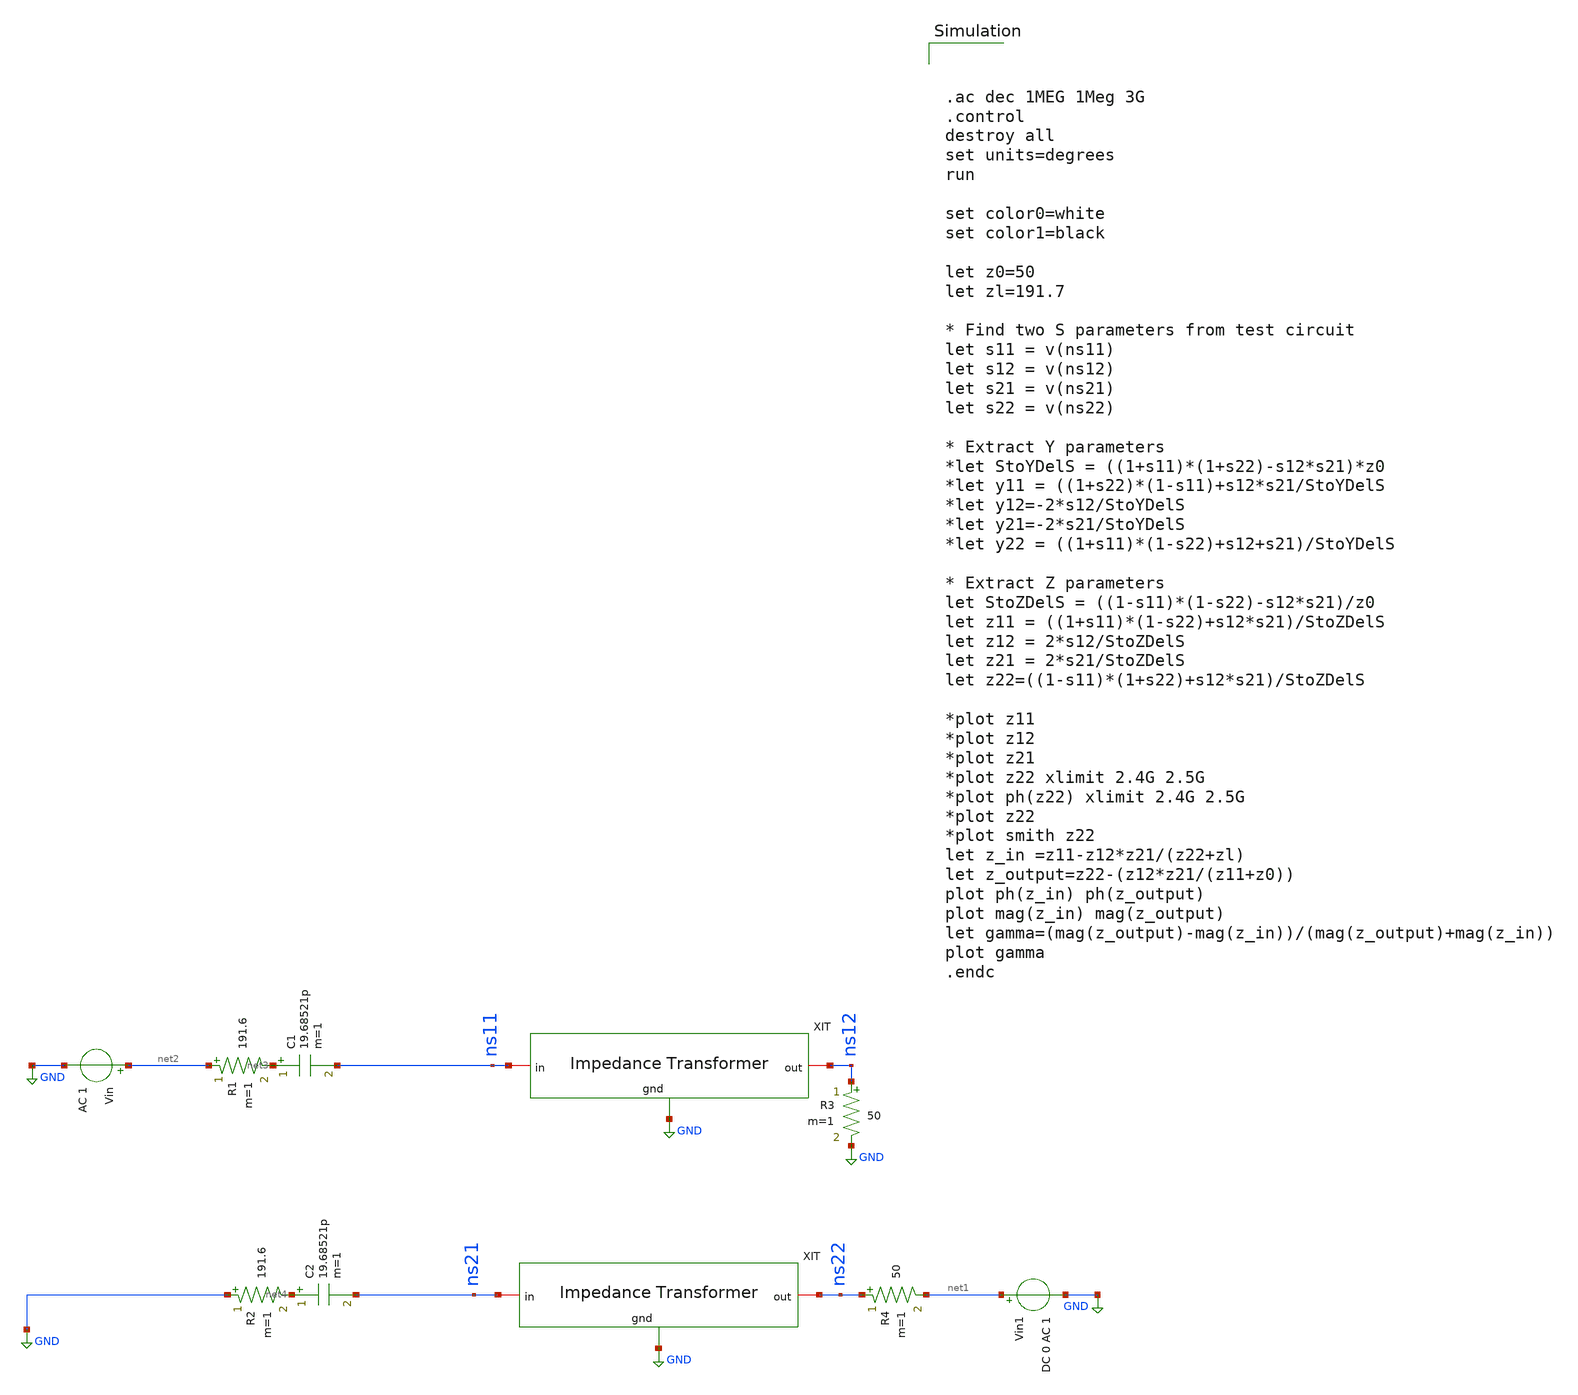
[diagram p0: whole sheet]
** sch_path: impedance-transformer/xschem/impedance-transformer_tb-ac.sch
**.subckt impedance-transformer_tb-ac
Vin1 net1 GND DC 0 AC 1
R3 ns12 GND 50 m=1
R4 ns22 net1 50 m=1
Vin net2 GND AC 1
R1 net2 net3 191.6 m=1
C1 net3 ns11 19.68521p m=1
R2 GND net4 191.6 m=1
C2 net4 ns21 19.68521p m=1
x1 ns11 ns12 GND impedance-transformer
x2 ns21 ns22 GND impedance-transformer
**** begin user architecture code



.ac dec 1MEG 1Meg 3G
.control
destroy all
set units=degrees
run

set color0=white
set color1=black

let z0=50
let zl=191.7

* Find two S parameters from test circuit
let s11 = v(ns11)
let s12 = v(ns12)
let s21 = v(ns21)
let s22 = v(ns22)

* Extract Y parameters
*let StoYDelS = ((1+s11)*(1+s22)-s12*s21)*z0
*let y11 = ((1+s22)*(1-s11)+s12*s21/StoYDelS
*let y12=-2*s12/StoYDelS
*let y21=-2*s21/StoYDelS
*let y22 = ((1+s11)*(1-s22)+s12+s21)/StoYDelS

* Extract Z parameters
let StoZDelS = ((1-s11)*(1-s22)-s12*s21)/z0
let z11 = ((1+s11)*(1-s22)+s12*s21)/StoZDelS
let z12 = 2*s12/StoZDelS
let z21 = 2*s21/StoZDelS
let z22=((1-s11)*(1+s22)+s12*s21)/StoZDelS

*plot z11
*plot z12
*plot z21
*plot z22 xlimit 2.4G 2.5G
*plot ph(z22) xlimit 2.4G 2.5G
*plot z22
*plot smith z22
let z_in =z11-z12*z21/(z22+zl)
let z_output=z22-(z12*z21/(z11+z0))
plot ph(z_in) ph(z_output)
plot mag(z_in) mag(z_output)
let gamma=(mag(z_output)-mag(z_in))/(mag(z_output)+mag(z_in))
plot gamma
.endc


.lib /home/hugodg/sky130_workspace/skywater-pdk/libraries/sky130_fd_pr_ngspice/latest/models/sky130.lib.spice tt

**** end user architecture code
**.ends

* expanding   symbol:
*+  /home/hugodg/projects-sky130/temp-sensor/impedance-transformer/xschem/impedance-transformer.sym # of pins=3
** sym_path: impedance-transformer/xschem/impedance-transformer.sym
** sch_path: impedance-transformer/xschem/impedance-transformer.sch
.subckt impedance-transformer in out gnd
*.iopin gnd
*.iopin in
*.iopin out
XC0 in gnd sky130_fd_pr__cap_mim_m3_2 W=22.93 L=22.93 MF=9 m=9
XC1 out gnd sky130_fd_pr__cap_mim_m3_2 W=24.07 L=24.07 MF=16 m=16
x1 in out l1
.ends


* expanding   symbol:  /home/hugodg/projects-sky130/temp-sensor/impedance-transformer/xschem/l1.sym
*+ # of pins=2
** sym_path: impedance-transformer/xschem/l1.sym
** sch_path: impedance-transformer/xschem/l1.sch
.subckt l1 p1 p2
*.iopin p2
*.iopin p1
L0 p1 net3 598p m=1
Cs1 p1 net1 26.59f m=1
Cs2 p2 net2 25.14f m=1
Rs1 net1 GND 63.55 m=1
Rs2 net2 GND 19.11 m=1
R1 p2 net3 2.89 m=1
.ends

.GLOBAL GND
.end
